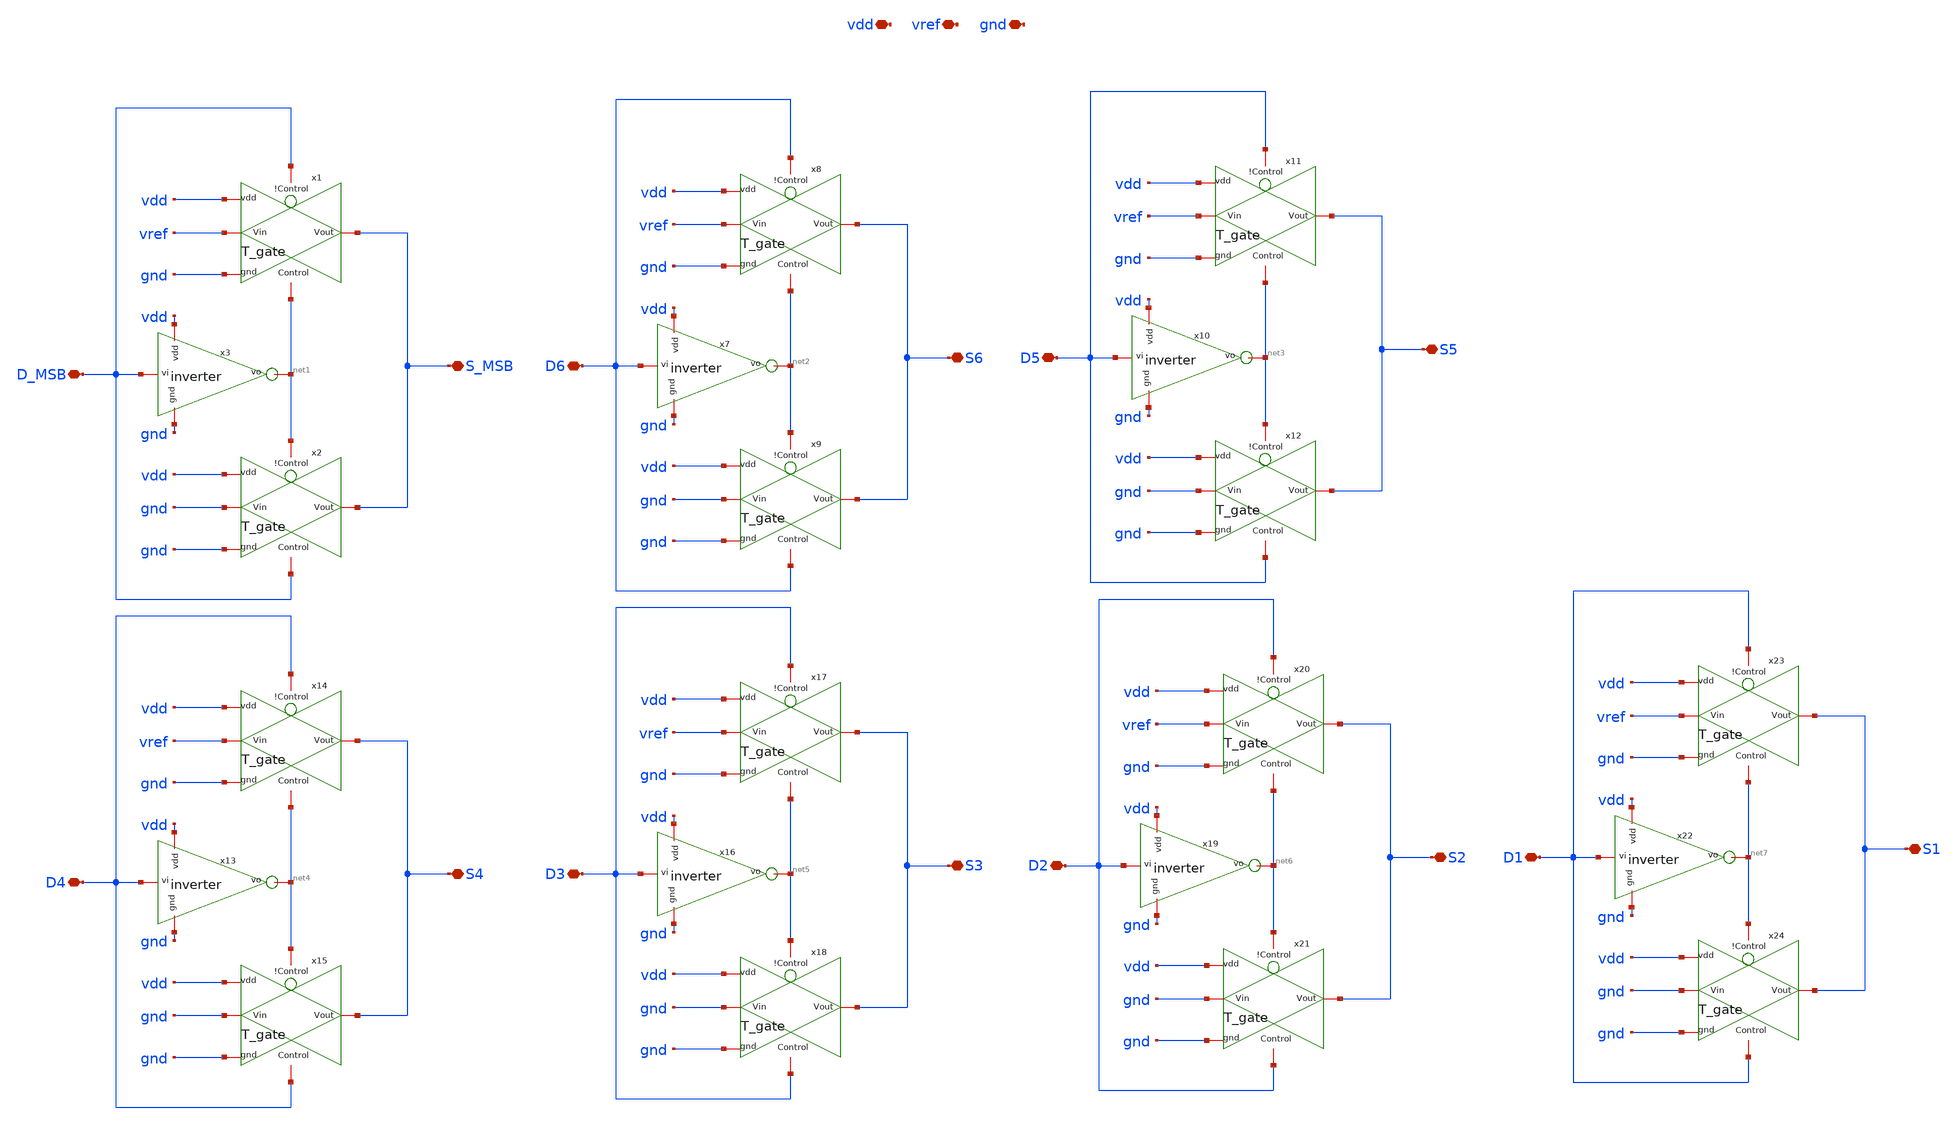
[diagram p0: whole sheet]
** sch_path: modules/module_3_8_bit_SAR_ADC/part_3_array_components/switch_array/switch_array.sch
**.subckt switch_array S_MSB S6 D_MSB D6 S5 D5 S4 S3 S2 D4 D3 D2 S1 D1 vdd vref gnd
*.iopin S_MSB
*.iopin S6
*.iopin D_MSB
*.iopin D6
*.iopin S5
*.iopin D5
*.iopin S4
*.iopin S3
*.iopin S2
*.iopin D4
*.iopin D3
*.iopin D2
*.iopin S1
*.iopin D1
*.iopin vdd
*.iopin vref
*.iopin gnd
x3 vdd D_MSB net1 gnd inverter
x1 D_MSB vref S_MSB gnd net1 vdd T_gate
x2 net1 gnd S_MSB gnd D_MSB vdd T_gate
x7 vdd D6 net2 gnd inverter
x8 D6 vref S6 gnd net2 vdd T_gate
x9 net2 gnd S6 gnd D6 vdd T_gate
x10 vdd D5 net3 gnd inverter
x11 D5 vref S5 gnd net3 vdd T_gate
x12 net3 gnd S5 gnd D5 vdd T_gate
x13 vdd D4 net4 gnd inverter
x14 D4 vref S4 gnd net4 vdd T_gate
x15 net4 gnd S4 gnd D4 vdd T_gate
x16 vdd D3 net5 gnd inverter
x17 D3 vref S3 gnd net5 vdd T_gate
x18 net5 gnd S3 gnd D3 vdd T_gate
x19 vdd D2 net6 gnd inverter
x20 D2 vref S2 gnd net6 vdd T_gate
x21 net6 gnd S2 gnd D2 vdd T_gate
x22 vdd D1 net7 gnd inverter
x23 D1 vref S1 gnd net7 vdd T_gate
x24 net7 gnd S1 gnd D1 vdd T_gate
**.ends

* expanding   symbol:
*+  /home/pedersen/projects/IHP-AnalogAcademy/modules/module_3_8_bit_SAR_ADC/part_2_digital_comps/bootstrap_switch/schematic/inverter.sym # of pins=4
** sym_path: modules/module_3_8_bit_SAR_ADC/part_2_digital_comps/bootstrap_switch/schematic/inverter.sym
** sch_path: modules/module_3_8_bit_SAR_ADC/part_2_digital_comps/bootstrap_switch/schematic/inverter.sch
.subckt inverter vdd vi vo gnd
*.iopin vi
*.iopin vo
*.iopin gnd
*.iopin vdd
XM5 vo vi vdd vdd sg13_lv_pmos w=800n l=130n ng=1 m=1 mm_ok=1
XM7 vo vi gnd gnd sg13_lv_nmos w=400n l=130n ng=1 m=1 mm_ok=1
.ends


* expanding   symbol:
*+  /home/pedersen/projects/IHP-AnalogAcademy/modules/module_3_8_bit_SAR_ADC/part_2_digital_comps/T_gate/schematic/T_gate.sym # of pins=6
** sym_path: modules/module_3_8_bit_SAR_ADC/part_2_digital_comps/T_gate/schematic/T_gate.sym
** sch_path: modules/module_3_8_bit_SAR_ADC/part_2_digital_comps/T_gate/schematic/T_gate.sch
.subckt T_gate !Control Vin Vout gnd Control vdd
*.iopin Vout
*.iopin Vin
*.iopin !Control
*.iopin Control
*.iopin gnd
*.iopin vdd
XM1 Vin Control Vout gnd sg13_lv_nmos w=1u l=0.13u ng=1 m=1 mm_ok=1
XM2 Vin !Control Vout vdd sg13_lv_pmos w=2u l=0.13u ng=1 m=1 mm_ok=1
.ends

.end
